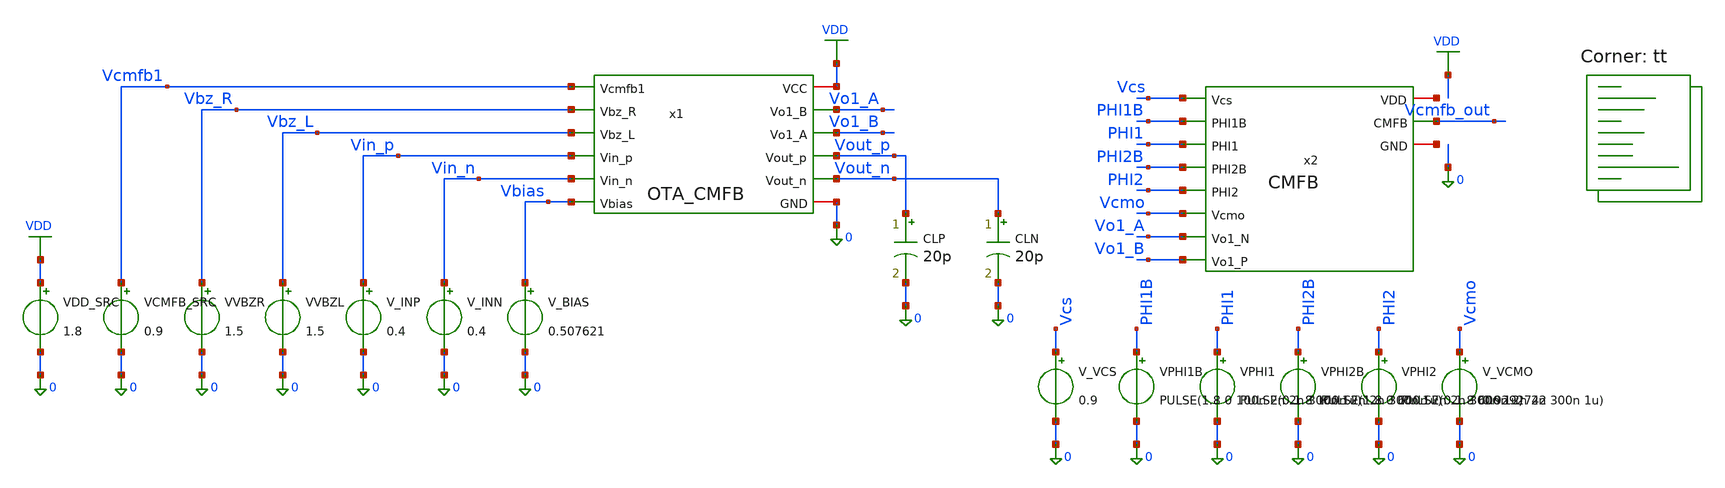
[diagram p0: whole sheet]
** sch_path: blocks/02_CMFB/sim/tb_OTA_baseline_CMFB_brokenloop.sch
**.subckt tb_OTA_baseline_CMFB_brokenloop
x1 VDD Vcmfb1 Vbz_R Vbz_L Vin_p Vin_n Vo1_A Vo1_B Vout_p Vout_n Vbias 0 OTA_CMFB
x2 Vcmfb_out Vcs PHI1B PHI1 net1 PHI2B net2 PHI2 Vcmo Vo1_A Vo1_B CMFB
VDD_SRC VDD 0 1.8
VCMFB_SRC Vcmfb1 0 0.9
VVBZR Vbz_R 0 1.5
VVBZL Vbz_L 0 1.5
V_INP Vin_p 0 0.4
V_INN Vin_n 0 0.4
V_BIAS Vbias 0 0.507621
CLP Vout_p 0 20p m=1
CLN Vout_n 0 20p m=1
V_VCS Vcs 0 0.9
VPHI1B PHI1B 0 PULSE(1.8 0 100n 2n 2n 300n 1u)
VPHI1 PHI1 0 PULSE(0 1.8 100n 2n 2n 300n 1u)
VPHI2B PHI2B 0 PULSE(1.8 0 600n 2n 2n 300n 1u)
VPHI2 PHI2 0 PULSE(0 1.8 600n 2n 2n 300n 1u)
V_VCMO Vcmo 0 0.9292742
**** begin user architecture code
.lib $::SKYWATER_MODELS/sky130.lib.spice tt


.options rshunt=1e12

RLEAK_CMFB Vcmfb_out 0 1e12

.control
save all

* ==========================================================
* OTA_CMFB + SC-CMFB FIRST-STAGE BROKEN-LOOP TEST
*
* Feedback loop is intentionally OPEN:
*
* VCMFB_SRC = 0.9 V drives OTA Vcmfb1.
* SC-CMFB output Vcmfb_out is only observed.
*
* SC-CMFB senses the TRUE first-stage nodes:
* Vo1_A and Vo1_B.
* ==========================================================

tran 1n 10u


* ==========================================================
* FIRST-STAGE OTA MEASUREMENTS
* ==========================================================

meas tran VO1A_AVG AVG v(vo1_a) FROM=8u TO=10u
meas tran VO1B_AVG AVG v(vo1_b) FROM=8u TO=10u
meas tran VO1A_MIN MIN v(vo1_a) FROM=8u TO=10u
meas tran VO1A_MAX MAX v(vo1_a) FROM=8u TO=10u
meas tran VO1B_MIN MIN v(vo1_b) FROM=8u TO=10u
meas tran VO1B_MAX MAX v(vo1_b) FROM=8u TO=10u

let VO1CM_AVG = (VO1A_AVG+VO1B_AVG)/2
let VO1D_AVG  = VO1A_AVG-VO1B_AVG
let VO1CM_ERROR = VO1CM_AVG-0.9292742


* ==========================================================
* FINAL OTA OUTPUT MEASUREMENTS
* ==========================================================

meas tran VOUTP_AVG AVG v(vout_p) FROM=8u TO=10u
meas tran VOUTN_AVG AVG v(vout_n) FROM=8u TO=10u

let VOCM_AVG = (VOUTP_AVG+VOUTN_AVG)/2
let VOD_AVG  = VOUTP_AVG-VOUTN_AVG


* ==========================================================
* BROKEN-LOOP CONTROL / CMFB OUTPUT
* ==========================================================

meas tran VCMFB_IN_AVG AVG v(vcmfb1) FROM=8u TO=10u

meas tran VCMFB_OUT_AVG AVG v(vcmfb_out) FROM=8u TO=10u
meas tran VCMFB_OUT_MIN MIN v(vcmfb_out) FROM=8u TO=10u
meas tran VCMFB_OUT_MAX MAX v(vcmfb_out) FROM=8u TO=10u

let VCMFB_OUT_RIPPLE = VCMFB_OUT_MAX-VCMFB_OUT_MIN
let VCMFB_TARGET_ERROR = VCMFB_OUT_AVG-0.9
let VCMFB_INTERFACE_ERROR = VCMFB_OUT_AVG-VCMFB_IN_AVG


* ==========================================================
* CLOCK CHECKS
* ==========================================================

meas tran PHI1_MAX MAX v(phi1)
meas tran PHI1_MIN MIN v(phi1)

meas tran PHI1B_MAX MAX v(phi1b)
meas tran PHI1B_MIN MIN v(phi1b)

meas tran PHI2_MAX MAX v(phi2)
meas tran PHI2_MIN MIN v(phi2)

meas tran PHI2B_MAX MAX v(phi2b)
meas tran PHI2B_MIN MIN v(phi2b)


* ==========================================================
* PRINT FIRST-STAGE RESULTS
* ==========================================================

echo
echo ===================================================
echo ===== FIRST-STAGE BROKEN-LOOP RESULTS =============
echo ===================================================

print VO1A_AVG
print VO1B_AVG
print VO1CM_AVG
print VO1D_AVG
print VO1CM_ERROR

print VO1A_MIN
print VO1A_MAX
print VO1B_MIN
print VO1B_MAX


* ==========================================================
* PRINT FINAL OTA OUTPUT RESULTS
* ==========================================================

echo
echo ===================================================
echo ===== FINAL OTA OUTPUT RESULTS ====================
echo ===================================================

print VOUTP_AVG
print VOUTN_AVG
print VOCM_AVG
print VOD_AVG


* ==========================================================
* PRINT SC-CMFB RESULTS
* ==========================================================

echo
echo ===================================================
echo ===== SC-CMFB BROKEN-LOOP RESULTS =================
echo ===================================================

print VCMFB_IN_AVG
print VCMFB_OUT_AVG
print VCMFB_OUT_MIN
print VCMFB_OUT_MAX
print VCMFB_OUT_RIPPLE
print VCMFB_TARGET_ERROR
print VCMFB_INTERFACE_ERROR


* ==========================================================
* PRINT CLOCK RESULTS
* ==========================================================

print PHI1_MAX
print PHI1_MIN
print PHI1B_MAX
print PHI1B_MIN

print PHI2_MAX
print PHI2_MIN
print PHI2B_MAX
print PHI2B_MIN


* ==========================================================
* WAVEFORMS
* ==========================================================

let VO1CM_TRACE = (v(vo1_a)+v(vo1_b))/2
let VOCM_TRACE = (v(vout_p)+v(vout_n))/2

plot v(phi1) v(phi2)
plot v(phi1b) v(phi2b)

plot v(vo1_a) v(vo1_b)
plot VO1CM_TRACE

plot v(vcmfb1) v(vcmfb_out)

plot v(vout_p) v(vout_n)
plot VOCM_TRACE

.endc


**** end user architecture code
**.ends
.GLOBAL VDD
.end
